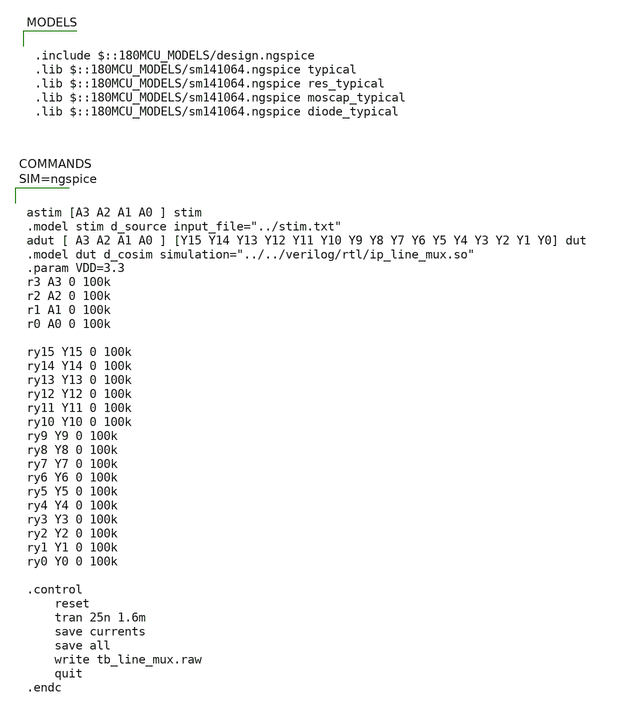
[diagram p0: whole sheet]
** sch_path: xschem/tb_line_mux.sch
**.subckt tb_line_mux
**** begin user architecture code

.include $::180MCU_MODELS/design.ngspice
.lib $::180MCU_MODELS/sm141064.ngspice typical
.lib $::180MCU_MODELS/sm141064.ngspice res_typical
.lib $::180MCU_MODELS/sm141064.ngspice moscap_typical
.lib $::180MCU_MODELS/sm141064.ngspice diode_typical




astim [A3 A2 A1 A0 ] stim
.model stim d_source input_file="../stim.txt"
adut [ A3 A2 A1 A0 ] [Y15 Y14 Y13 Y12 Y11 Y10 Y9 Y8 Y7 Y6 Y5 Y4 Y3 Y2 Y1 Y0] dut
.model dut d_cosim simulation="../../verilog/rtl/ip_line_mux.so"
.param VDD=3.3
r3 A3 0 100k
r2 A2 0 100k
r1 A1 0 100k
r0 A0 0 100k

ry15 Y15 0 100k
ry14 Y14 0 100k
ry13 Y13 0 100k
ry12 Y12 0 100k
ry11 Y11 0 100k
ry10 Y10 0 100k
ry9 Y9 0 100k
ry8 Y8 0 100k
ry7 Y7 0 100k
ry6 Y6 0 100k
ry5 Y5 0 100k
ry4 Y4 0 100k
ry3 Y3 0 100k
ry2 Y2 0 100k
ry1 Y1 0 100k
ry0 Y0 0 100k

.control
	reset
	tran 25n 1.6m
	save currents
	save all
	write tb_line_mux.raw
	quit
.endc



**** end user architecture code
**.ends
.end
